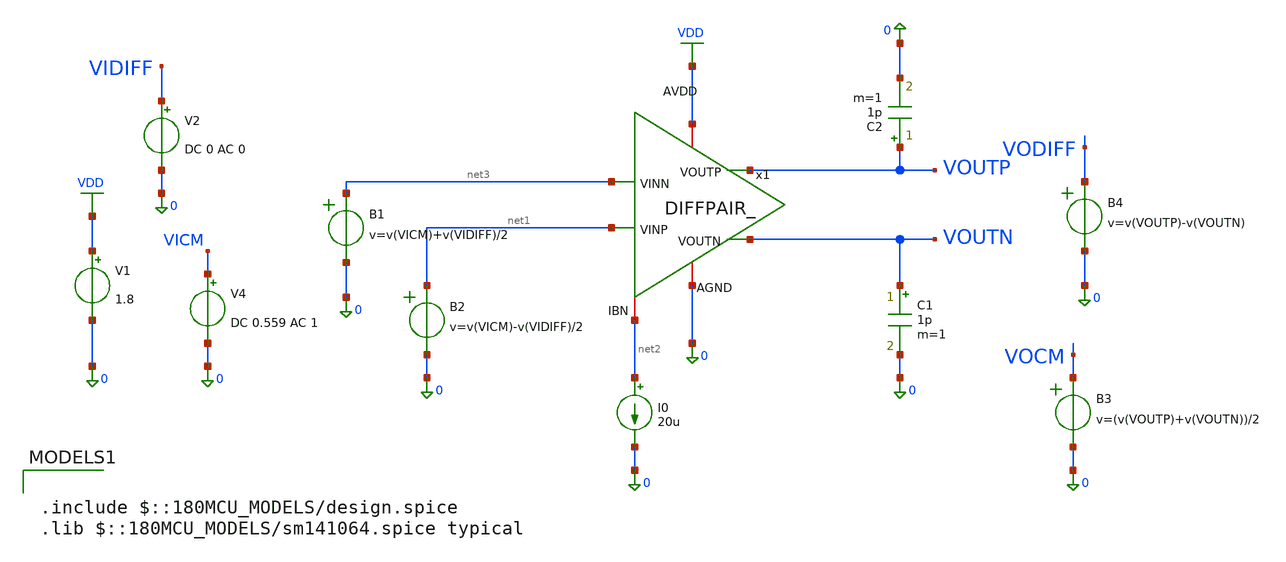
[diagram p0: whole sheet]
** sch_path: Lab_03/lab_06.sch
**.subckt lab_06
V1 VDD 0 1.8
V4 VICM 0 DC 0.559 AC 1
V2 VIDIFF 0 DC 0 AC 0
B1 net3 0 v=v(VICM)+v(VIDIFF)/2
B2 net1 0 v=v(VICM)-v(VIDIFF)/2
B3 VOCM 0 v=(v(VOUTP)+v(VOUTN))/2
B4 VODIFF 0 v=v(VOUTP)-v(VOUTN)
I0 net2 0 20u
C1 VOUTN 0 1p m=1
C2 VOUTP 0 1p m=1
x1 net2 net3 0 net1 VDD VOUTP VOUTN DIFFPAIR WP1=40.32u LP1=810.8n WP2=30u LP2=350n RD=30K
**** begin user architecture code

.include $::180MCU_MODELS/design.spice
.lib $::180MCU_MODELS/sm141064.spice typical




.control
alterparam sw_stat_global = 0
alterparam sw_stat_mismatch = 0
reset
save all
let x = 1
set num = {$&x}
dowhile x <= 4
save @m.x1.xm{$num}.m0[id]
save @m.x1.xm{$num}.m0[vgs]
save @m.x1.xm{$num}.m0[vds]
save @m.x1.xm{$num}.m0[vdsat]
save @m.x1.xm{$num}.m0[vth]
save @m.x1.xm{$num}.m0[gm]
save @m.x1.xm{$num}.m0[gds]
save @m.x1.xm{$num}.m0[gmbs]
save @m.x1.xm{$num}.m0[cgg]
save @m.x1.xm{$num}.m0[cdd]
save @m.x1.xm{$num}.m0[css]
let x = x + 1
set num = {$&x}



end
* === OP Point ===
op
write lab_06.raw
set appendwrite
echo " === MOSFET Operating Points ==="
show m : id : vgs : vds : vth : vdsat : gm : gds : gmbs
echo " === Bias Points ==="
let x = 1
dowhile x <= 4
set num = {$&x}
let gmid = @m.x1.xm{$num}.m0[gm]/@m.x1.xm{$num}.m0[id]
let Vstar = 2/gmid
echo "M{$num}: gm/id = $&gmid S/A, Vstar = $&Vstar V"
let x = x + 1
end
* === DIFFERENTIAL AC ===
alter V2 AC = 1
alter V4 AC = 0
ac dec 10 1 10e9
write lab_06_ac_diff.raw
write lab_06.raw
* === COMMON MODE AC ===
alter V2 AC = 0
alter V4 AC = 1
ac dec 10 1 10e9
write lab_06_ac_cm.raw
write lab_06.raw
* === EXTRACT RESULTS ===
set units=degrees
let vod = ac1.v(VODIFF)
let vocm = ac2.v(VOCM)
let CMRR = vdb(vod) - vdb(vocm)
* === MEASUREMENTS ===
meas ac Av_diff_db find vdb(vod) at=1
meas ac Av_diff_mag find vmag(vod) at=1
let A3db = Av_diff_mag/sqrt(2)
meas ac BW_diff when vmag(vod)=A3db fall=1
meas ac Av_CM_db find vdb(vocm) at=1
meas ac Av_CM_mag find vmag(vocm) at=1
let A3db = Av_CM_mag/sqrt(2)
meas ac BW_CM when vmag(vocm)=A3db fall=1
let CMRR_db = Av_diff_db - Av_CM_db
* === DISPLAY RESULTS ===
echo " === AC Results ==="
echo "Av Diff: $&Av_diff_db dB, BW: $&BW_diff Hz"
echo "Av CM: $&Av_CM_db dB, BW: $&BW_CM Hz"
echo "CMRR: $&CMRR_db dB"
write lab_06.raw
.endc

**** end user architecture code
**.ends

* expanding   symbol:  DIFFPAIR.sym # of pins=7
** sym_path: Lab_03/DIFFPAIR.sym
** sch_path: Lab_03/DIFFPAIR.sch
.subckt DIFFPAIR IBN VINN AGND VINP AVDD VOUTP VOUTN  WP1=1u LP1=0.5u WP2=1u LP2=0.5u RD=1k
*.iopin IBN
*.iopin AGND
*.iopin AVDD
*.ipin VINN
*.ipin VINP
*.opin VOUTP
*.opin VOUTN
XM3 IBN IBN AVDD AVDD pfet_03v3 L={LP1} W={WP1} nf=1 ad='int((nf+1)/2) * W/nf * 0.18u' as='int((nf+2)/2) * W/nf * 0.18u'
+ pd='2*int((nf+1)/2) * (W/nf + 0.18u)' ps='2*int((nf+2)/2) * (W/nf + 0.18u)' nrd='0.18u / W' nrs='0.18u / W'
+ sa=0 sb=0 sd=0 m=1
XM4 VOUTP VINN net1 AVDD pfet_03v3 L={LP2} W={WP2} nf=1 ad='int((nf+1)/2) * W/nf * 0.18u' as='int((nf+2)/2) * W/nf * 0.18u'
+ pd='2*int((nf+1)/2) * (W/nf + 0.18u)' ps='2*int((nf+2)/2) * (W/nf + 0.18u)' nrd='0.18u / W' nrs='0.18u / W'
+ sa=0 sb=0 sd=0 m=1
R1 VOUTN AGND {RD} m=1
R2 VOUTP AGND {RD} m=1
XM1 VOUTN VINP net1 AVDD pfet_03v3 L={LP2} W={WP2} nf=1 ad='int((nf+1)/2) * W/nf * 0.18u' as='int((nf+2)/2) * W/nf * 0.18u'
+ pd='2*int((nf+1)/2) * (W/nf + 0.18u)' ps='2*int((nf+2)/2) * (W/nf + 0.18u)' nrd='0.18u / W' nrs='0.18u / W'
+ sa=0 sb=0 sd=0 m=1
XM2 net1 IBN AVDD AVDD pfet_03v3 L={LP1} W={2*WP1} nf=1 ad='int((nf+1)/2) * W/nf * 0.18u' as='int((nf+2)/2) * W/nf * 0.18u'
+ pd='2*int((nf+1)/2) * (W/nf + 0.18u)' ps='2*int((nf+2)/2) * (W/nf + 0.18u)' nrd='0.18u / W' nrs='0.18u / W'
+ sa=0 sb=0 sd=0 m=1
.ends

.GLOBAL VDD
.end
